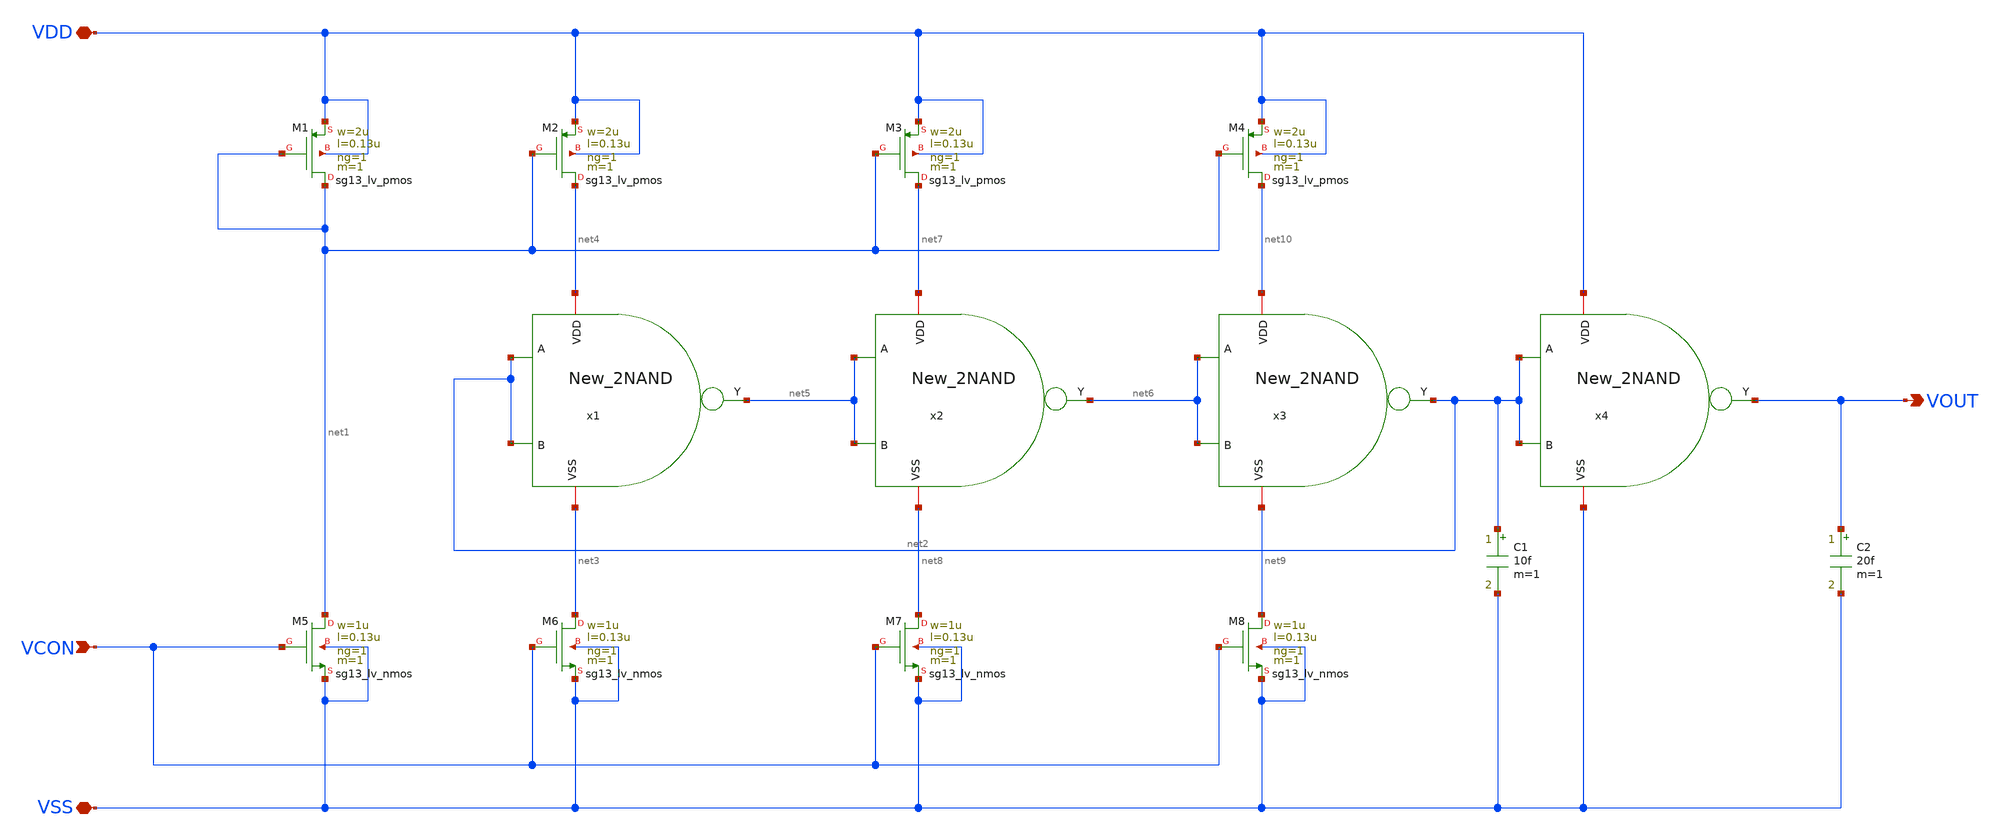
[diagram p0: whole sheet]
** sch_path: Team 1 Design/design_data/xschem/VCO/VCO_3Stages.sch
**.subckt VCO_3Stages VDD VSS VCON VOUT
*.iopin VDD
*.iopin VSS
*.ipin VCON
*.opin VOUT
XM1 net1 net1 VDD VDD sg13_lv_pmos w=2u l=0.13u ng=1 m=1 mm_ok=1
XM2 net4 net1 VDD VDD sg13_lv_pmos w=2u l=0.13u ng=1 m=1 mm_ok=1
XM3 net7 net1 VDD VDD sg13_lv_pmos w=2u l=0.13u ng=1 m=1 mm_ok=1
XM4 net10 net1 VDD VDD sg13_lv_pmos w=2u l=0.13u ng=1 m=1 mm_ok=1
XM5 net1 VCON VSS VSS sg13_lv_nmos w=1u l=0.13u ng=1 m=1 mm_ok=1
XM6 net3 VCON VSS VSS sg13_lv_nmos w=1u l=0.13u ng=1 m=1 mm_ok=1
XM7 net8 VCON VSS VSS sg13_lv_nmos w=1u l=0.13u ng=1 m=1 mm_ok=1
XM8 net9 VCON VSS VSS sg13_lv_nmos w=1u l=0.13u ng=1 m=1 mm_ok=1
C1 net2 VSS 10f m=1
C2 VOUT VSS 20f m=1
x1 net4 net3 net2 net5 net2 New_2NAND
x2 net7 net8 net5 net6 net5 New_2NAND
x3 net10 net9 net6 net2 net6 New_2NAND
x4 VDD VSS net2 VOUT net2 New_2NAND
**.ends

* expanding   symbol:  /foss/designs/Team1/New_2NAND/New_2NAND.sym # of pins=5
** sym_path: Team 1 Design/design_data/xschem/2_Input_NAND_New/New_2NAND.sym
** sch_path: Team 1 Design/design_data/xschem/2_Input_NAND_New/New_2NAND.sch
.subckt New_2NAND VDD VSS A Y B
*.ipin B
*.opin Y
*.ipin A
*.iopin VDD
*.iopin VSS
XM1 Y A VDD VDD sg13_lv_pmos w=3u l=0.13u ng=1 m=1 mm_ok=1
XM2 Y B VDD VDD sg13_lv_pmos w=3u l=0.13u ng=1 m=1 mm_ok=1
XM3 Y B net1 VSS sg13_lv_nmos w=2u l=0.13u ng=1 m=1 mm_ok=1
XM4 net1 A VSS VSS sg13_lv_nmos w=2u l=0.13u ng=1 m=1 mm_ok=1
.ends

.end
